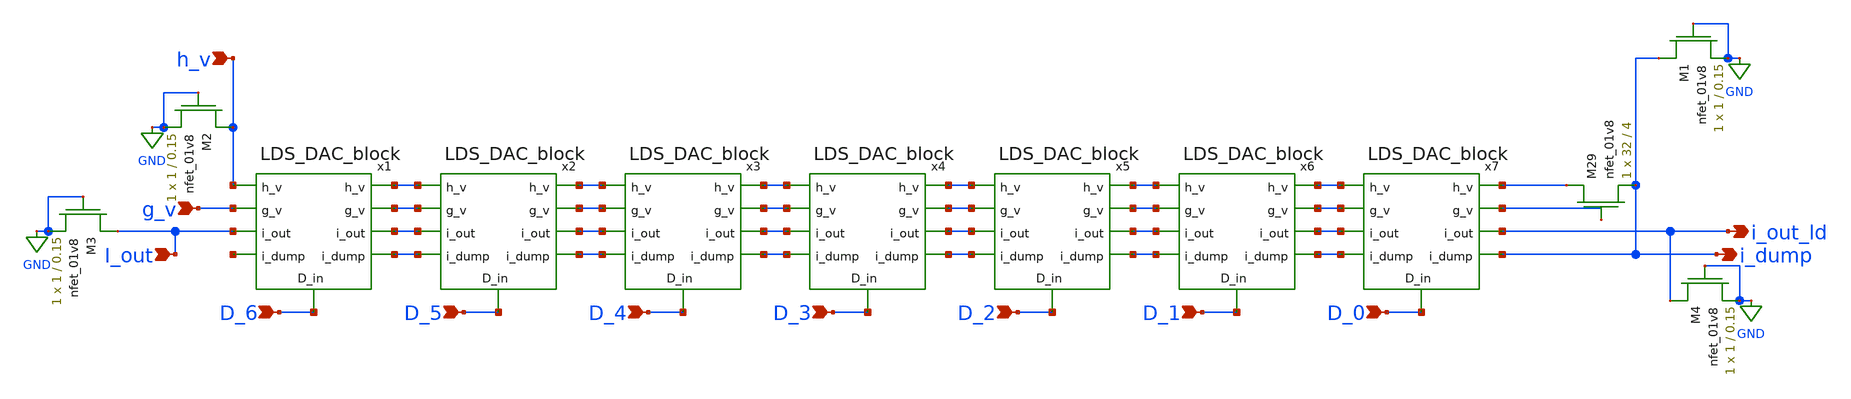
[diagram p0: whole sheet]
** sch_path: schemas/7bit_DAC_LDS.sch
**.subckt 7bit_DAC_LDS i_out_ld i_dump g_v D_6 D_5 D_4 D_3 D_2 D_1 D_0 h_v I_out
*.opin i_out_ld
*.opin i_dump
*.ipin g_v
*.ipin D_6
*.ipin D_5
*.ipin D_4
*.ipin D_3
*.ipin D_2
*.ipin D_1
*.ipin D_0
*.ipin h_v
*.ipin I_out
x1 h_v g_v i_out_ld i_dump D_6 LDS_DAC_block
x2 h_v g_v i_out_ld i_dump D_5 LDS_DAC_block
x3 h_v g_v i_out_ld i_dump D_4 LDS_DAC_block
x4 h_v g_v i_out_ld i_dump D_3 LDS_DAC_block
x5 h_v g_v i_out_ld i_dump D_2 LDS_DAC_block
x6 h_v g_v i_out_ld i_dump D_1 LDS_DAC_block
x7 h_v g_v i_out_ld i_dump D_0 LDS_DAC_block
XM29 h_v g_v i_dump GND sky130_fd_pr__nfet_01v8 L=4 W=32 nf=1 ad='int((nf+1)/2) * W/nf * 0.29' as='int((nf+2)/2) * W/nf * 0.29'
+ pd='2*int((nf+1)/2) * (W/nf + 0.29)' ps='2*int((nf+2)/2) * (W/nf + 0.29)' nrd='0.29 / W' nrs='0.29 / W'
+ sa=0 sb=0 sd=0 mult=1 m=1
XM2 h_v GND GND GND sky130_fd_pr__nfet_01v8 L=0.15 W=1 nf=1 ad='int((nf+1)/2) * W/nf * 0.29' as='int((nf+2)/2) * W/nf * 0.29'
+ pd='2*int((nf+1)/2) * (W/nf + 0.29)' ps='2*int((nf+2)/2) * (W/nf + 0.29)' nrd='0.29 / W' nrs='0.29 / W'
+ sa=0 sb=0 sd=0 mult=1 m=1
XM3 i_out_ld GND GND GND sky130_fd_pr__nfet_01v8 L=0.15 W=1 nf=1 ad='int((nf+1)/2) * W/nf * 0.29' as='int((nf+2)/2) * W/nf * 0.29'
+ pd='2*int((nf+1)/2) * (W/nf + 0.29)' ps='2*int((nf+2)/2) * (W/nf + 0.29)' nrd='0.29 / W' nrs='0.29 / W'
+ sa=0 sb=0 sd=0 mult=1 m=1
XM1 i_dump GND GND GND sky130_fd_pr__nfet_01v8 L=0.15 W=1 nf=1 ad='int((nf+1)/2) * W/nf * 0.29' as='int((nf+2)/2) * W/nf * 0.29'
+ pd='2*int((nf+1)/2) * (W/nf + 0.29)' ps='2*int((nf+2)/2) * (W/nf + 0.29)' nrd='0.29 / W' nrs='0.29 / W'
+ sa=0 sb=0 sd=0 mult=1 m=1
XM4 i_out_ld GND GND GND sky130_fd_pr__nfet_01v8 L=0.15 W=1 nf=1 ad='int((nf+1)/2) * W/nf * 0.29' as='int((nf+2)/2) * W/nf * 0.29'
+ pd='2*int((nf+1)/2) * (W/nf + 0.29)' ps='2*int((nf+2)/2) * (W/nf + 0.29)' nrd='0.29 / W' nrs='0.29 / W'
+ sa=0 sb=0 sd=0 mult=1 m=1
**.ends

* expanding   symbol:  /home/lxbtlr/MADVLSI-MP4-DAC/schemas/LDS_DAC_block.sym # of pins=9
** sym_path: /home/lxbtlr/MADVLSI-MP4-DAC/schemas/LDS_DAC_block.sym
** sch_path: /home/lxbtlr/MADVLSI-MP4-DAC/schemas/LDS_DAC_block.sch
.subckt LDS_DAC_block h_v g_v i_out i_dump D_in
*.opin i_dump
*.opin i_out
*.opin g_v
*.opin h_v
*.ipin g_v
*.ipin i_out
*.ipin i_dump
*.ipin h_v
*.ipin D_in
XM13 h_v g_v net1 GND sky130_fd_pr__nfet_01v8 L=4 W=32 nf=1 ad='int((nf+1)/2) * W/nf * 0.29' as='int((nf+2)/2) * W/nf * 0.29'
+ pd='2*int((nf+1)/2) * (W/nf + 0.29)' ps='2*int((nf+2)/2) * (W/nf + 0.29)' nrd='0.29 / W' nrs='0.29 / W'
+ sa=0 sb=0 sd=0 mult=1 m=1
XM14 i_out D_in h_v GND sky130_fd_pr__nfet_01v8 L=4 W=32 nf=1 ad='int((nf+1)/2) * W/nf * 0.29' as='int((nf+2)/2) * W/nf * 0.29'
+ pd='2*int((nf+1)/2) * (W/nf + 0.29)' ps='2*int((nf+2)/2) * (W/nf + 0.29)' nrd='0.29 / W' nrs='0.29 / W'
+ sa=0 sb=0 sd=0 mult=1 m=1
XM15 net1 g_v h_v GND sky130_fd_pr__nfet_01v8 L=4 W=32 nf=1 ad='int((nf+1)/2) * W/nf * 0.29' as='int((nf+2)/2) * W/nf * 0.29'
+ pd='2*int((nf+1)/2) * (W/nf + 0.29)' ps='2*int((nf+2)/2) * (W/nf + 0.29)' nrd='0.29 / W' nrs='0.29 / W'
+ sa=0 sb=0 sd=0 mult=1 m=1
XM16 h_v net2 i_dump GND sky130_fd_pr__nfet_01v8 L=4 W=32 nf=1 ad='int((nf+1)/2) * W/nf * 0.29' as='int((nf+2)/2) * W/nf * 0.29'
+ pd='2*int((nf+1)/2) * (W/nf + 0.29)' ps='2*int((nf+2)/2) * (W/nf + 0.29)' nrd='0.29 / W' nrs='0.29 / W'
+ sa=0 sb=0 sd=0 mult=1 m=1
XM19 net2 D_in GND GND sky130_fd_pr__nfet_01v8 L=1 W=.15 nf=1 ad='int((nf+1)/2) * W/nf * 0.29' as='int((nf+2)/2) * W/nf * 0.29'
+ pd='2*int((nf+1)/2) * (W/nf + 0.29)' ps='2*int((nf+2)/2) * (W/nf + 0.29)' nrd='0.29 / W' nrs='0.29 / W'
+ sa=0 sb=0 sd=0 mult=1 m=1
XM20 net2 D_in VDD VDD sky130_fd_pr__pfet_01v8 L=1 W=.30 nf=1 ad='int((nf+1)/2) * W/nf * 0.29' as='int((nf+2)/2) * W/nf * 0.29'
+ pd='2*int((nf+1)/2) * (W/nf + 0.29)' ps='2*int((nf+2)/2) * (W/nf + 0.29)' nrd='0.29 / W' nrs='0.29 / W'
+ sa=0 sb=0 sd=0 mult=1 m=1
.ends

.GLOBAL GND
.GLOBAL VDD
.end
